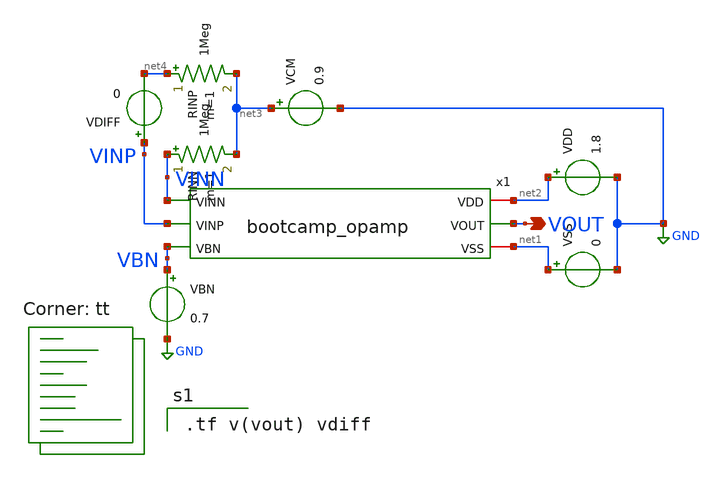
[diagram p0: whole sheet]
** sch_path: analog/bootcamp_opamp/schematics/tb_impedance.sch
**.subckt tb_impedance VOUT
*.opin VOUT
x1 VINN net2 net1 VINP VOUT VBN bootcamp_opamp
VDD net2 GND 1.8
VSS net1 GND 0
VCM net3 GND 0.9
RINP net4 net3 1Meg m=1
RINN VINN net3 1Meg m=1
VDIFF VINP net4 0
VBN VBN GND 0.7
**** begin user architecture code
.lib $::SKYWATER_MODELS/sky130.lib.spice tt

.tf v(vout) vdiff

**** end user architecture code
**.ends
.GLOBAL GND
.end
